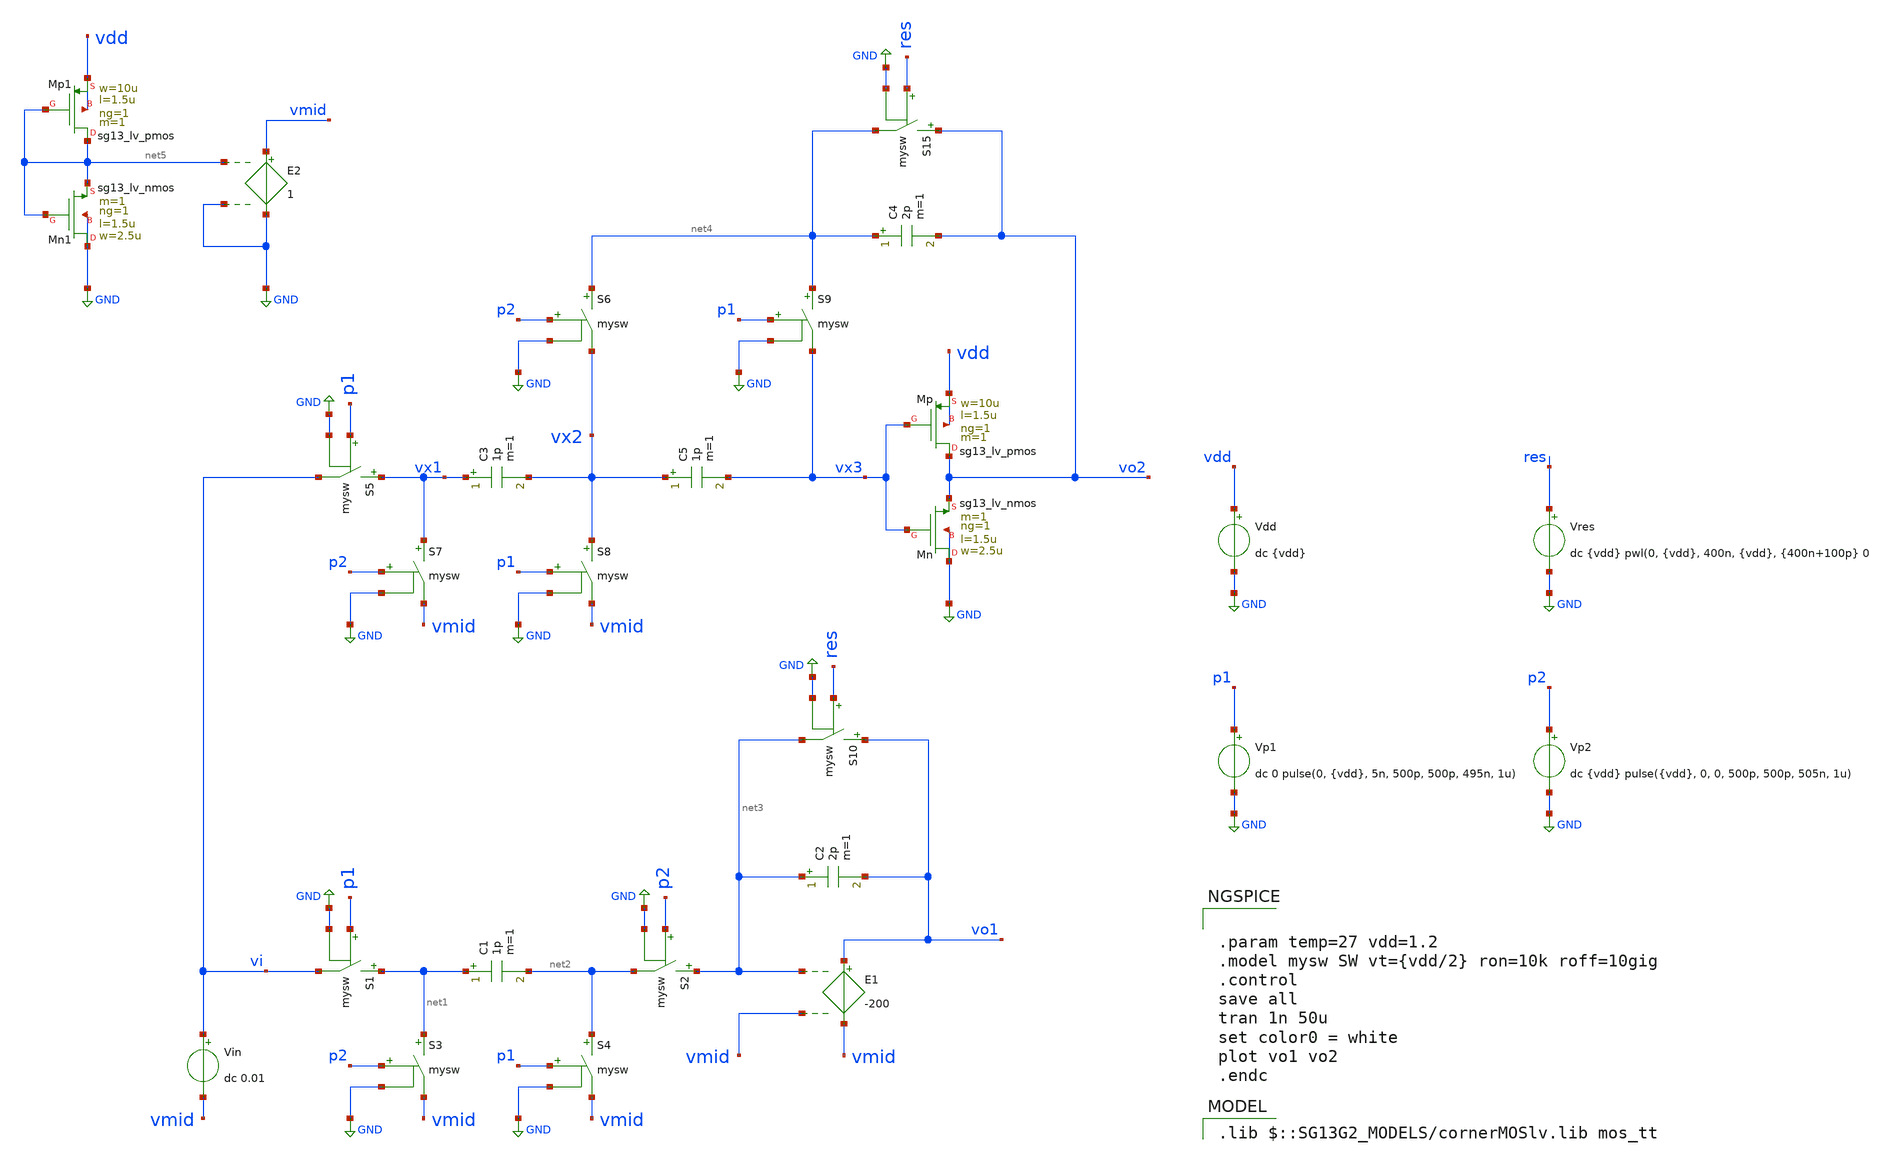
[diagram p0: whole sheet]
** sch_path: 5_Design/3_Real_circuits/sandbox_boris/tb_chae_integ_inv.sch
**.subckt tb_chae_integ_inv
Vp1 p1 GND dc 0 pulse(0, {vdd}, 5n, 500p, 500p, 495n, 1u)
E1 vo1 vmid net3 vmid -200
S1 net1 vi p1 GND mysw
Vp2 p2 GND dc {vdd} pulse({vdd}, 0, 0, 500p, 500p, 505n, 1u)
Vin vi vmid dc 0.01
C1 net1 net2 1p m=1
S2 net3 net2 p2 GND mysw
C2 net3 vo1 2p m=1
S3 net1 vmid p2 GND mysw
S4 net2 vmid p1 GND mysw
S5 vx1 vi p1 GND mysw
C3 vx1 vx2 1p m=1
C4 net4 vo2 2p m=1
S7 vx1 vmid p2 GND mysw
S8 vx2 vmid p1 GND mysw
C5 vx2 vx3 1p m=1
S6 net4 vx2 p2 GND mysw
S9 net4 vx3 p1 GND mysw
Vdd vdd GND dc {vdd}
XMn GND vx3 vo2 GND sg13_lv_nmos w=2.5u l=1.5u ng=1 m=1 mm_ok=1
XMp vo2 vx3 vdd vdd sg13_lv_pmos w=10u l=1.5u ng=1 m=1 mm_ok=1
S15 vo2 net4 res GND mysw
Vres res GND dc {vdd} pwl(0, {vdd}, 400n, {vdd}, {400n+100p} 0
XMn1 GND net5 net5 GND sg13_lv_nmos w=2.5u l=1.5u ng=1 m=1 mm_ok=1
XMp1 net5 net5 vdd vdd sg13_lv_pmos w=10u l=1.5u ng=1 m=1 mm_ok=1
E2 vmid GND net5 GND 1
S10 vo1 net3 res GND mysw
**** begin user architecture code


.param temp=27 vdd=1.2
.model mysw SW vt={vdd/2} ron=10k roff=10gig
.control
save all
tran 1n 50u
set color0 = white
plot vo1 vo2
.endc


 .lib $::SG13G2_MODELS/cornerMOSlv.lib mos_tt

**** end user architecture code
**.ends
.GLOBAL GND
.end
